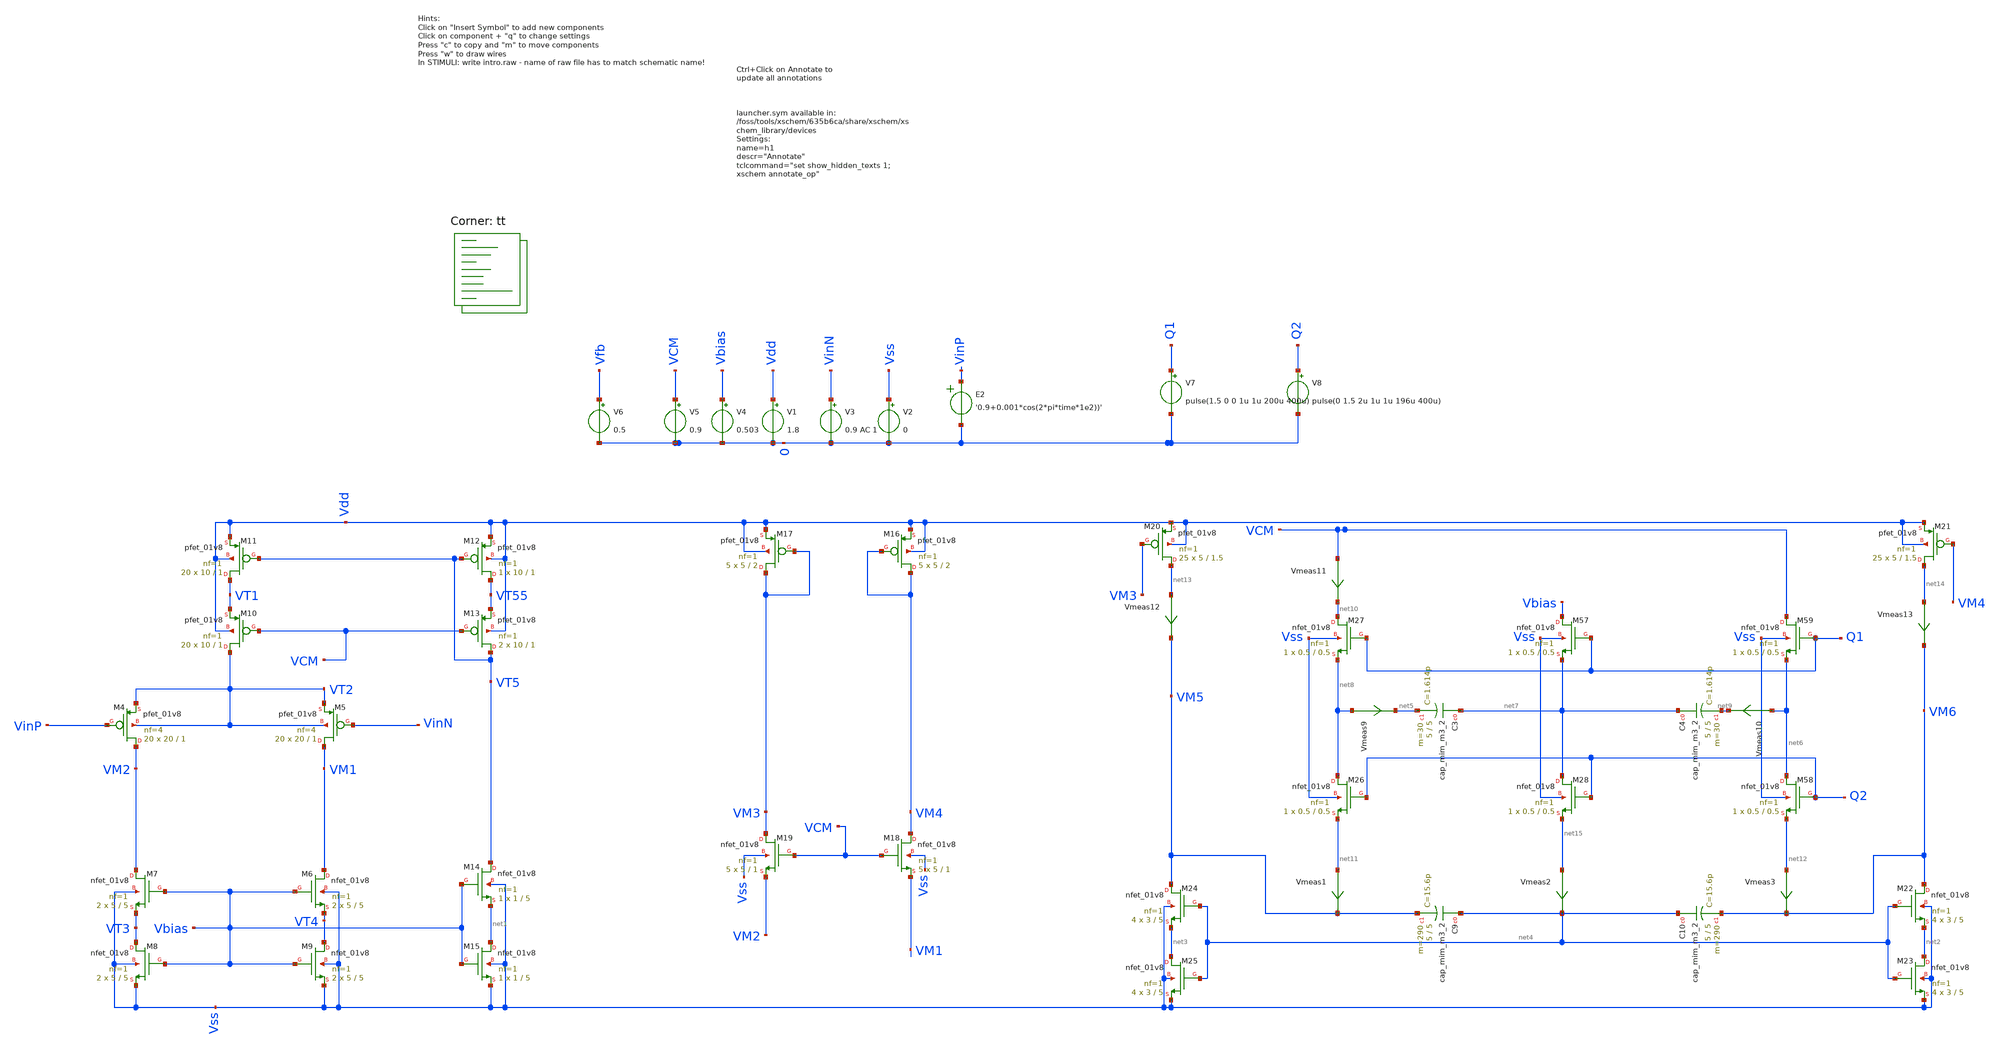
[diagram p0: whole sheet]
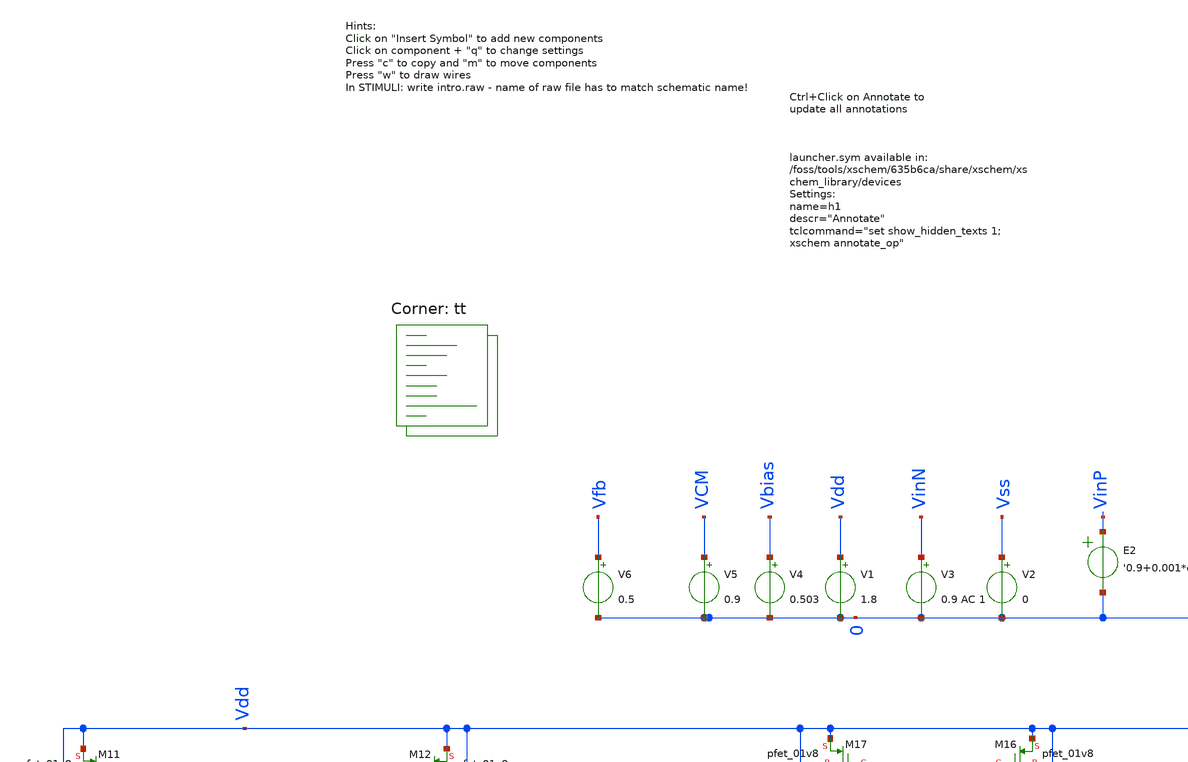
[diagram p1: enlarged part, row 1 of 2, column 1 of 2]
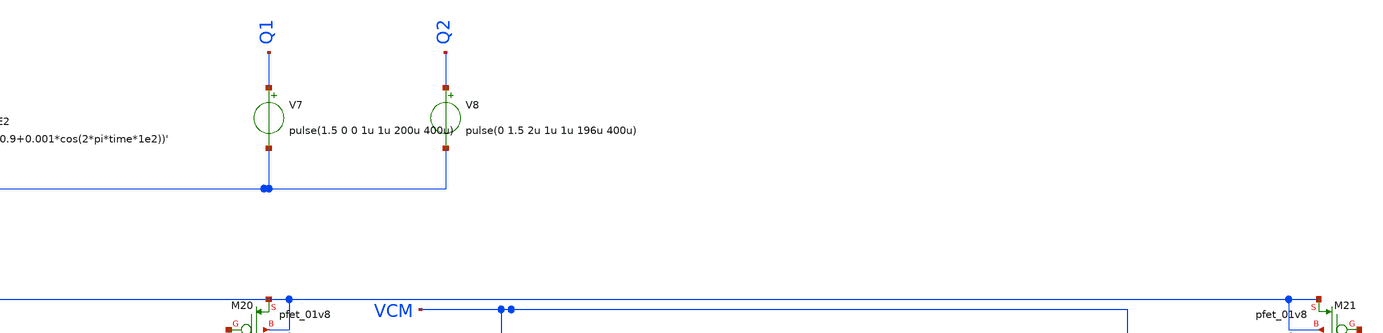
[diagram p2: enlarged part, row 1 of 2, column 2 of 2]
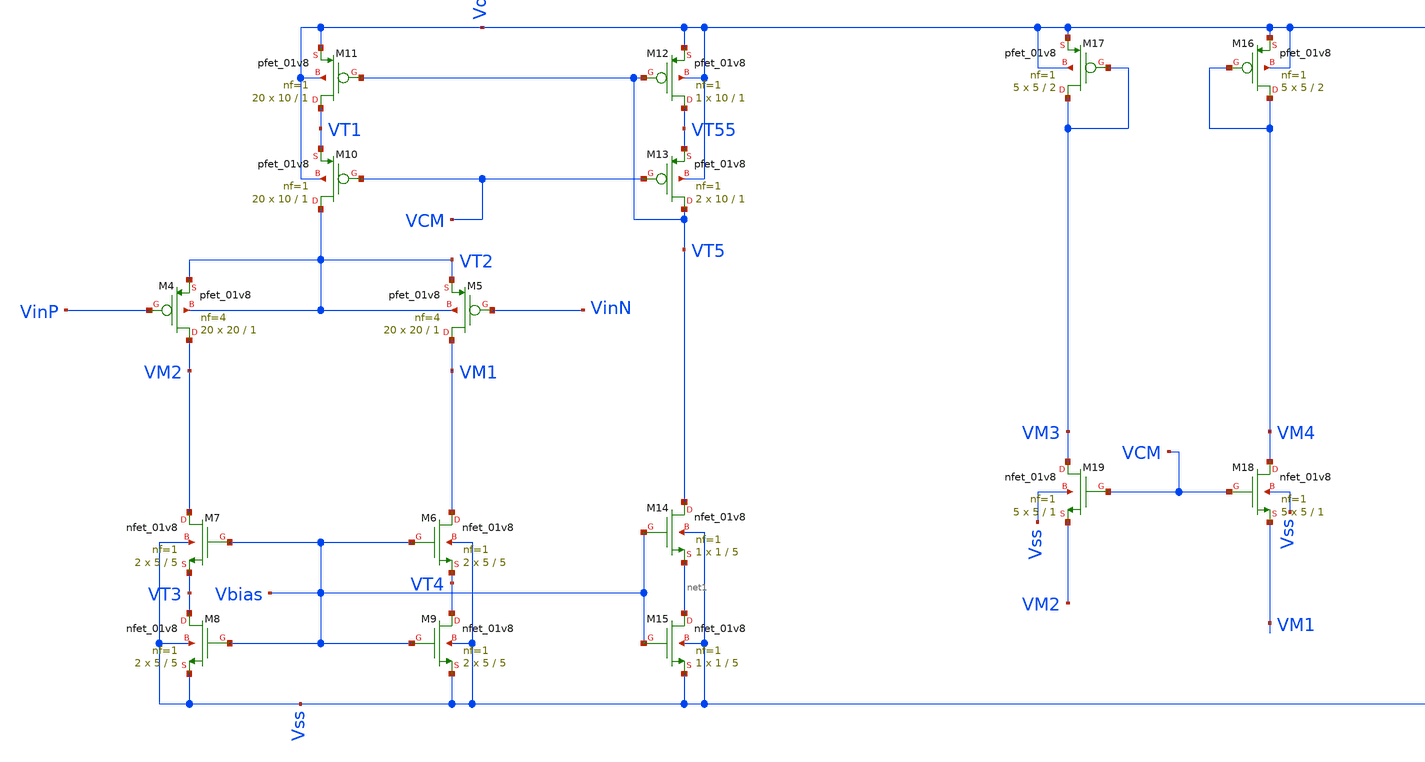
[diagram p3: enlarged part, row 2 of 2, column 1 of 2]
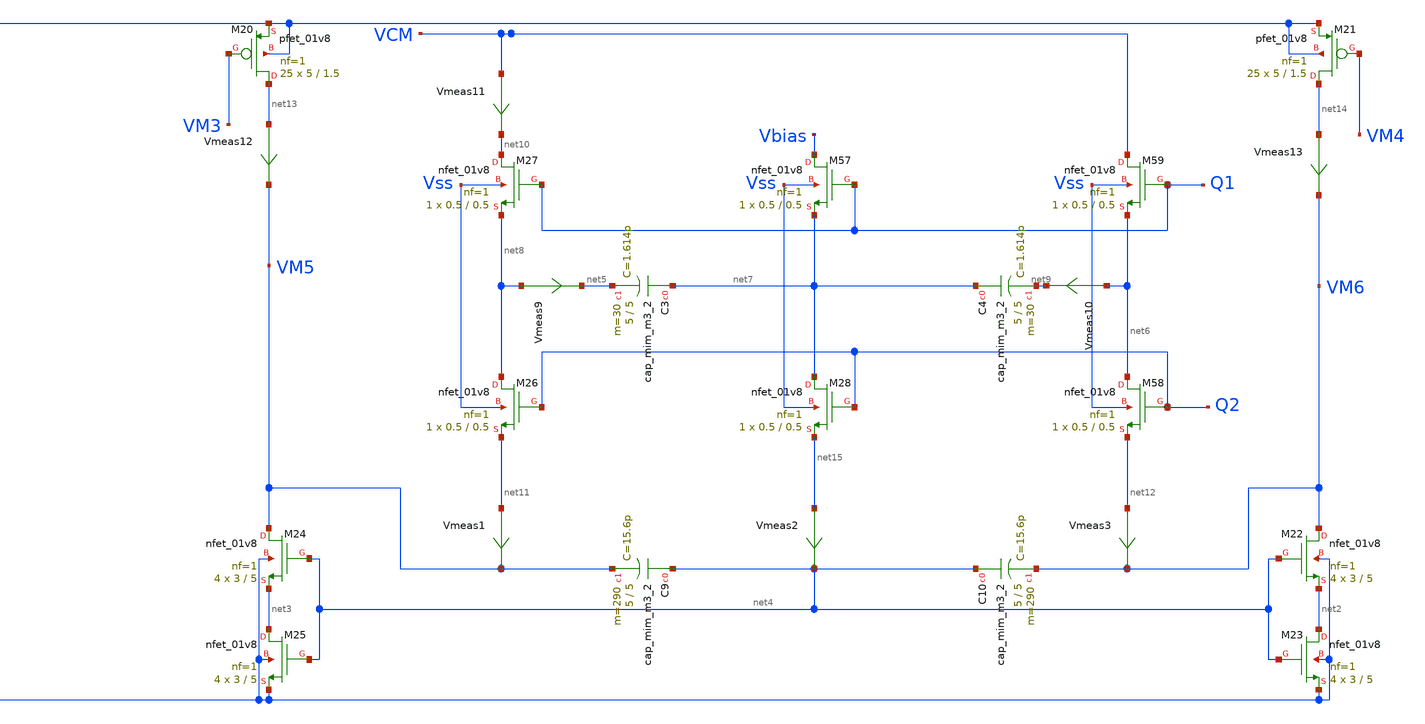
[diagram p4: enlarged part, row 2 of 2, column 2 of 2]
** sch_path: Back-up15-01.sch
**.subckt Back-up15-01
XM4 VM2 VinP VT2 VT2 sky130_fd_pr__pfet_01v8 L=1 W=20 nf=4 ad='int((nf+1)/2) * W/nf * 0.29' as='int((nf+2)/2) * W/nf * 0.29'
+ pd='2*int((nf+1)/2) * (W/nf + 0.29)' ps='2*int((nf+2)/2) * (W/nf + 0.29)' nrd='0.29 / W' nrs='0.29 / W'
+ sa=0 sb=0 sd=0 mult=20 m=20
XM5 VM1 VinN VT2 VT2 sky130_fd_pr__pfet_01v8 L=1 W=20 nf=4 ad='int((nf+1)/2) * W/nf * 0.29' as='int((nf+2)/2) * W/nf * 0.29'
+ pd='2*int((nf+1)/2) * (W/nf + 0.29)' ps='2*int((nf+2)/2) * (W/nf + 0.29)' nrd='0.29 / W' nrs='0.29 / W'
+ sa=0 sb=0 sd=0 mult=20 m=20
XM6 VM1 Vbias VT4 Vss sky130_fd_pr__nfet_01v8 L=5 W=5 nf=1 ad='int((nf+1)/2) * W/nf * 0.29' as='int((nf+2)/2) * W/nf * 0.29'
+ pd='2*int((nf+1)/2) * (W/nf + 0.29)' ps='2*int((nf+2)/2) * (W/nf + 0.29)' nrd='0.29 / W' nrs='0.29 / W'
+ sa=0 sb=0 sd=0 mult=2 m=2
XM7 VM2 Vbias VT3 Vss sky130_fd_pr__nfet_01v8 L=5 W=5 nf=1 ad='int((nf+1)/2) * W/nf * 0.29' as='int((nf+2)/2) * W/nf * 0.29'
+ pd='2*int((nf+1)/2) * (W/nf + 0.29)' ps='2*int((nf+2)/2) * (W/nf + 0.29)' nrd='0.29 / W' nrs='0.29 / W'
+ sa=0 sb=0 sd=0 mult=2 m=2
XM8 VT3 Vbias Vss Vss sky130_fd_pr__nfet_01v8 L=5 W=5 nf=1 ad='int((nf+1)/2) * W/nf * 0.29' as='int((nf+2)/2) * W/nf * 0.29'
+ pd='2*int((nf+1)/2) * (W/nf + 0.29)' ps='2*int((nf+2)/2) * (W/nf + 0.29)' nrd='0.29 / W' nrs='0.29 / W'
+ sa=0 sb=0 sd=0 mult=2 m=2
XM9 VT4 Vbias Vss Vss sky130_fd_pr__nfet_01v8 L=5 W=5 nf=1 ad='int((nf+1)/2) * W/nf * 0.29' as='int((nf+2)/2) * W/nf * 0.29'
+ pd='2*int((nf+1)/2) * (W/nf + 0.29)' ps='2*int((nf+2)/2) * (W/nf + 0.29)' nrd='0.29 / W' nrs='0.29 / W'
+ sa=0 sb=0 sd=0 mult=2 m=2
XM10 VT2 VCM VT1 Vdd sky130_fd_pr__pfet_01v8 L=1 W=10 nf=1 ad='int((nf+1)/2) * W/nf * 0.29' as='int((nf+2)/2) * W/nf * 0.29'
+ pd='2*int((nf+1)/2) * (W/nf + 0.29)' ps='2*int((nf+2)/2) * (W/nf + 0.29)' nrd='0.29 / W' nrs='0.29 / W'
+ sa=0 sb=0 sd=0 mult=20 m=20
XM11 VT1 VT5 Vdd Vdd sky130_fd_pr__pfet_01v8 L=1 W=10 nf=1 ad='int((nf+1)/2) * W/nf * 0.29' as='int((nf+2)/2) * W/nf * 0.29'
+ pd='2*int((nf+1)/2) * (W/nf + 0.29)' ps='2*int((nf+2)/2) * (W/nf + 0.29)' nrd='0.29 / W' nrs='0.29 / W'
+ sa=0 sb=0 sd=0 mult=20 m=20
XM12 VT55 VT5 Vdd Vdd sky130_fd_pr__pfet_01v8 L=1 W=10 nf=1 ad='int((nf+1)/2) * W/nf * 0.29' as='int((nf+2)/2) * W/nf * 0.29'
+ pd='2*int((nf+1)/2) * (W/nf + 0.29)' ps='2*int((nf+2)/2) * (W/nf + 0.29)' nrd='0.29 / W' nrs='0.29 / W'
+ sa=0 sb=0 sd=0 mult=1 m=1
XM13 VT5 VCM VT55 Vdd sky130_fd_pr__pfet_01v8 L=1 W=10 nf=1 ad='int((nf+1)/2) * W/nf * 0.29' as='int((nf+2)/2) * W/nf * 0.29'
+ pd='2*int((nf+1)/2) * (W/nf + 0.29)' ps='2*int((nf+2)/2) * (W/nf + 0.29)' nrd='0.29 / W' nrs='0.29 / W'
+ sa=0 sb=0 sd=0 mult=2 m=2
XM14 VT5 Vbias net1 Vss sky130_fd_pr__nfet_01v8 L=5 W=1 nf=1 ad='int((nf+1)/2) * W/nf * 0.29' as='int((nf+2)/2) * W/nf * 0.29'
+ pd='2*int((nf+1)/2) * (W/nf + 0.29)' ps='2*int((nf+2)/2) * (W/nf + 0.29)' nrd='0.29 / W' nrs='0.29 / W'
+ sa=0 sb=0 sd=0 mult=1 m=1
XM15 net1 Vbias Vss Vss sky130_fd_pr__nfet_01v8 L=5 W=1 nf=1 ad='int((nf+1)/2) * W/nf * 0.29' as='int((nf+2)/2) * W/nf * 0.29'
+ pd='2*int((nf+1)/2) * (W/nf + 0.29)' ps='2*int((nf+2)/2) * (W/nf + 0.29)' nrd='0.29 / W' nrs='0.29 / W'
+ sa=0 sb=0 sd=0 mult=1 m=1
XM16 VM4 VM4 Vdd Vdd sky130_fd_pr__pfet_01v8 L=2 W=5 nf=1 ad='int((nf+1)/2) * W/nf * 0.29' as='int((nf+2)/2) * W/nf * 0.29'
+ pd='2*int((nf+1)/2) * (W/nf + 0.29)' ps='2*int((nf+2)/2) * (W/nf + 0.29)' nrd='0.29 / W' nrs='0.29 / W'
+ sa=0 sb=0 sd=0 mult=5 m=5
XM17 VM3 VM3 Vdd Vdd sky130_fd_pr__pfet_01v8 L=2 W=5 nf=1 ad='int((nf+1)/2) * W/nf * 0.29' as='int((nf+2)/2) * W/nf * 0.29'
+ pd='2*int((nf+1)/2) * (W/nf + 0.29)' ps='2*int((nf+2)/2) * (W/nf + 0.29)' nrd='0.29 / W' nrs='0.29 / W'
+ sa=0 sb=0 sd=0 mult=5 m=5
XM18 VM4 VCM VM1 Vss sky130_fd_pr__nfet_01v8 L=1 W=5 nf=1 ad='int((nf+1)/2) * W/nf * 0.29' as='int((nf+2)/2) * W/nf * 0.29'
+ pd='2*int((nf+1)/2) * (W/nf + 0.29)' ps='2*int((nf+2)/2) * (W/nf + 0.29)' nrd='0.29 / W' nrs='0.29 / W'
+ sa=0 sb=0 sd=0 mult=5 m=5
XM19 VM3 VCM VM2 Vss sky130_fd_pr__nfet_01v8 L=1 W=5 nf=1 ad='int((nf+1)/2) * W/nf * 0.29' as='int((nf+2)/2) * W/nf * 0.29'
+ pd='2*int((nf+1)/2) * (W/nf + 0.29)' ps='2*int((nf+2)/2) * (W/nf + 0.29)' nrd='0.29 / W' nrs='0.29 / W'
+ sa=0 sb=0 sd=0 mult=5 m=5
XM20 net13 VM3 Vdd Vdd sky130_fd_pr__pfet_01v8 L=1.5 W=5 nf=1 ad='int((nf+1)/2) * W/nf * 0.29' as='int((nf+2)/2) * W/nf * 0.29'
+ pd='2*int((nf+1)/2) * (W/nf + 0.29)' ps='2*int((nf+2)/2) * (W/nf + 0.29)' nrd='0.29 / W' nrs='0.29 / W'
+ sa=0 sb=0 sd=0 mult=25 m=25
XM21 net14 VM4 Vdd Vdd sky130_fd_pr__pfet_01v8 L=1.5 W=5 nf=1 ad='int((nf+1)/2) * W/nf * 0.29' as='int((nf+2)/2) * W/nf * 0.29'
+ pd='2*int((nf+1)/2) * (W/nf + 0.29)' ps='2*int((nf+2)/2) * (W/nf + 0.29)' nrd='0.29 / W' nrs='0.29 / W'
+ sa=0 sb=0 sd=0 mult=25 m=25
XM22 VM6 net4 net2 Vss sky130_fd_pr__nfet_01v8 L=5 W=3 nf=1 ad='int((nf+1)/2) * W/nf * 0.29' as='int((nf+2)/2) * W/nf * 0.29'
+ pd='2*int((nf+1)/2) * (W/nf + 0.29)' ps='2*int((nf+2)/2) * (W/nf + 0.29)' nrd='0.29 / W' nrs='0.29 / W'
+ sa=0 sb=0 sd=0 mult=4 m=4
XM23 net2 net4 Vss Vss sky130_fd_pr__nfet_01v8 L=5 W=3 nf=1 ad='int((nf+1)/2) * W/nf * 0.29' as='int((nf+2)/2) * W/nf * 0.29'
+ pd='2*int((nf+1)/2) * (W/nf + 0.29)' ps='2*int((nf+2)/2) * (W/nf + 0.29)' nrd='0.29 / W' nrs='0.29 / W'
+ sa=0 sb=0 sd=0 mult=4 m=4
XM24 VM5 net4 net3 Vss sky130_fd_pr__nfet_01v8 L=5 W=3 nf=1 ad='int((nf+1)/2) * W/nf * 0.29' as='int((nf+2)/2) * W/nf * 0.29'
+ pd='2*int((nf+1)/2) * (W/nf + 0.29)' ps='2*int((nf+2)/2) * (W/nf + 0.29)' nrd='0.29 / W' nrs='0.29 / W'
+ sa=0 sb=0 sd=0 mult=4 m=4
XM25 net3 net4 Vss Vss sky130_fd_pr__nfet_01v8 L=5 W=3 nf=1 ad='int((nf+1)/2) * W/nf * 0.29' as='int((nf+2)/2) * W/nf * 0.29'
+ pd='2*int((nf+1)/2) * (W/nf + 0.29)' ps='2*int((nf+2)/2) * (W/nf + 0.29)' nrd='0.29 / W' nrs='0.29 / W'
+ sa=0 sb=0 sd=0 mult=4 m=4
E2 VinP 0 VOL=' '0.9+0.001*cos(2*pi*time*1e2))' '
V1 Vdd 0 1.8
V2 Vss 0 0
V3 VinN 0 0.9 AC 1
V4 Vbias 0 0.503
V5 VCM 0 0.9
V6 Vfb 0 0.5
XC3 net7 net5 sky130_fd_pr__cap_mim_m3_2 W=5 L=5 MF=30 m=30
XC4 net7 net9 sky130_fd_pr__cap_mim_m3_2 W=5 L=5 MF=30 m=30
XC9 net4 VM5 sky130_fd_pr__cap_mim_m3_2 W=5 L=5 MF=290 m=290
XC10 net4 VM6 sky130_fd_pr__cap_mim_m3_2 W=5 L=5 MF=290 m=290
XM26 net8 Q2 net11 Vss sky130_fd_pr__nfet_01v8 L=0.5 W=0.5 nf=1 ad='int((nf+1)/2) * W/nf * 0.29' as='int((nf+2)/2) * W/nf * 0.29'
+ pd='2*int((nf+1)/2) * (W/nf + 0.29)' ps='2*int((nf+2)/2) * (W/nf + 0.29)' nrd='0.29 / W' nrs='0.29 / W'
+ sa=0 sb=0 sd=0 mult=1 m=1
XM27 net10 Q1 net8 Vss sky130_fd_pr__nfet_01v8 L=0.5 W=0.5 nf=1 ad='int((nf+1)/2) * W/nf * 0.29' as='int((nf+2)/2) * W/nf * 0.29'
+ pd='2*int((nf+1)/2) * (W/nf + 0.29)' ps='2*int((nf+2)/2) * (W/nf + 0.29)' nrd='0.29 / W' nrs='0.29 / W'
+ sa=0 sb=0 sd=0 mult=1 m=1
XM28 net7 Q2 net15 Vss sky130_fd_pr__nfet_01v8 L=0.5 W=0.5 nf=1 ad='int((nf+1)/2) * W/nf * 0.29' as='int((nf+2)/2) * W/nf * 0.29'
+ pd='2*int((nf+1)/2) * (W/nf + 0.29)' ps='2*int((nf+2)/2) * (W/nf + 0.29)' nrd='0.29 / W' nrs='0.29 / W'
+ sa=0 sb=0 sd=0 mult=1 m=1
XM57 Vbias Q1 net7 Vss sky130_fd_pr__nfet_01v8 L=0.5 W=0.5 nf=1 ad='int((nf+1)/2) * W/nf * 0.29' as='int((nf+2)/2) * W/nf * 0.29'
+ pd='2*int((nf+1)/2) * (W/nf + 0.29)' ps='2*int((nf+2)/2) * (W/nf + 0.29)' nrd='0.29 / W' nrs='0.29 / W'
+ sa=0 sb=0 sd=0 mult=1 m=1
XM58 net6 Q2 net12 Vss sky130_fd_pr__nfet_01v8 L=0.5 W=0.5 nf=1 ad='int((nf+1)/2) * W/nf * 0.29' as='int((nf+2)/2) * W/nf * 0.29'
+ pd='2*int((nf+1)/2) * (W/nf + 0.29)' ps='2*int((nf+2)/2) * (W/nf + 0.29)' nrd='0.29 / W' nrs='0.29 / W'
+ sa=0 sb=0 sd=0 mult=1 m=1
XM59 VCM Q1 net6 Vss sky130_fd_pr__nfet_01v8 L=0.5 W=0.5 nf=1 ad='int((nf+1)/2) * W/nf * 0.29' as='int((nf+2)/2) * W/nf * 0.29'
+ pd='2*int((nf+1)/2) * (W/nf + 0.29)' ps='2*int((nf+2)/2) * (W/nf + 0.29)' nrd='0.29 / W' nrs='0.29 / W'
+ sa=0 sb=0 sd=0 mult=1 m=1
V7 Q1 0 pulse(1.5 0 0 1u 1u 200u 400u)
V8 Q2 0 pulse(0 1.5 2u 1u 1u 196u 400u)
Vmeas9 net8 net5 0
.save i(vmeas9)
Vmeas10 net6 net9 0
.save i(vmeas10)
Vmeas11 VCM net10 0
.save i(vmeas11)
Vmeas12 net13 VM5 0
.save i(vmeas12)
Vmeas13 net14 VM6 0
.save i(vmeas13)
Vmeas1 net11 VM5 0
.save i(vmeas1)
Vmeas2 net15 net4 0
.save i(vmeas2)
Vmeas3 net12 VM6 0
.save i(vmeas3)
**** begin user architecture code


.options savecurrents
.control



save all
save @m.xm1.msky130_fd_pr__nfet_01v8_lvt[id]
save @m.xm1.msky130_fd_pr__pfet_01v8[id]
save @m.xm7.msky130_fd_pr__pfet_01v8[id]
save @m.xm1.msky130_fd_pr__nfet_01v8_lvt[vth]
save @m.xm11.msky130_fd_pr__pfet_01v8[vth]
save @m.xm1.msky130_fd_pr__nfet_01v8_lvt[vgs]
save @m.xm1.msky130_fd_pr__nfet_01v8_lvt[vds]
save @m.xm1.msky130_fd_pr__nfet_01v8_lvt[gm]
save @m.xm1.msky130_fd_pr__nfet_01v8_lvt[gds]
save @m.xm23.msky130_fd_pr__nfet_01v8[cgs]
save @m.xm15.msky130_fd_pr__nfet_01v8[cgs]

save @m.xm1.msky130_fd_pr__pfet_01v8[id]
save @m.xm2.msky130_fd_pr__pfet_01v8_lvt[id]
save @m.xm2.msky130_fd_pr__pfet_01v8_lvt[vth]
save @m.xm1.msky130_fd_pr__pfet_01v8[vgs]
save @m.xm2.msky130_fd_pr__pfet_01v8_lvt[vds]
save @m.xm2.msky130_fd_pr__pfet_01v8_lvt[gm]
save @m.xm2.msky130_fd_pr__pfet_01v8_lvt[gds]
save @m.xm2.msky130_fd_pr__pfet_01v8_lvt[cgs]

op
remzerovec
write Back-up15-01.raw
*set appendwrite

*dc V1 0 1.8 0.01
*plot @m.xm1.msky130_fd_pr__nfet_01v8_lvt[id] @m.xm2.msky130_fd_pr__pfet_01v8_lvt[id]
*remzerovec
*write intro.raw

.endc
.control
tran 500u 1
save all
plot v(VM5)
plot v(VM6)-v(VM5)

*noise V(VM5,VM6) V1 dec 100 0.1 100
*print inoise_total onoise_total
*setplot noise1
*plot inoise_spectrum


.endc





.lib $::SKYWATER_MODELS/sky130.lib.spice tt
**** end user architecture code
**.ends
.end
